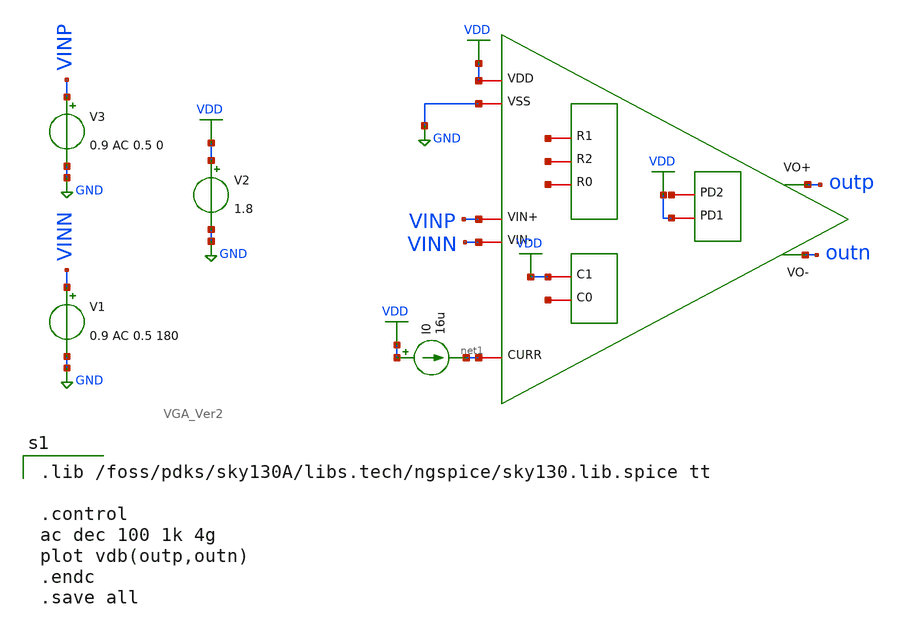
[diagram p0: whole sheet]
** sch_path: VGA/VGA_Ver2_tb.sch
**.subckt VGA_Ver2_tb
x1 outp outn net1 GND VDD VDD net2 VINN VINP net3 net4 net5 net6 VDD VGA_Ver2
V1 VINN GND 0.9 AC 0.5 180
V2 VDD GND 1.8
V3 VINP GND 0.9 AC 0.5 0
I0 VDD net1 16u
**** begin user architecture code

.lib /foss/pdks/sky130A/libs.tech/ngspice/sky130.lib.spice tt

.control
ac dec 100 1k 4g
plot vdb(outp,outn)
.endc
.save all


**** end user architecture code
**.ends

* expanding   symbol:  /foss/designs/VGA/VGA_Ver2.sym # of pins=14
** sym_path: VGA/VGA_Ver2.sym
** sch_path: VGA/VGA_Ver2.sch
.subckt VGA_Ver2 VO+ VO- CURR VSS VDD PD1 PD2 VIN- VIN+ R0 R2 R1 C0 C1
*.iopin VIN+
*.iopin VIN-
*.opin VO+
*.opin VO-
*.iopin VDD
*.iopin VSS
*.iopin PD1
*.iopin PD2
*.iopin CURR
*.iopin R0
*.iopin R1
*.iopin R2
*.iopin C1
*.iopin C0
XM10 net1 net9 VDD VDD sky130_fd_pr__pfet_01v8_lvt L=0.4 W=30 nf=1 ad='int((1 + 1)/2) * 30 / 1 * 0.29'
+ as='int((1 + 2)/2) * 30 / 1 * 0.29' pd='2*int((1 + 1)/2) * (30 / 1 + 0.29)' ps='2*int((1 + 2)/2) * (30 / 1 + 0.29)'
+ nrd='0.29 / 30 ' nrs='0.29 / 30 ' sa=0 sb=0 sd=0 mult=1 m=1
XM1 net2 net4 VDD VDD sky130_fd_pr__pfet_01v8_lvt L=0.4 W=30 nf=1 ad='int((1 + 1)/2) * 30 / 1 * 0.29'
+ as='int((1 + 2)/2) * 30 / 1 * 0.29' pd='2*int((1 + 1)/2) * (30 / 1 + 0.29)' ps='2*int((1 + 2)/2) * (30 / 1 + 0.29)'
+ nrd='0.29 / 30 ' nrs='0.29 / 30 ' sa=0 sb=0 sd=0 mult=1 m=1
RS net1 VO- 1000 m=1
RS1 net2 VO+ 1000 m=1
RS2 net9 VO- 1600 m=1
RS3 VO+ net4 1600 m=1
XM2 VO- VIN+ net10 VSS sky130_fd_pr__nfet_01v8_lvt L=0.2 W=11 nf=1 ad='int((1 + 1)/2) * 11 / 1 * 0.29'
+ as='int((1 + 2)/2) * 11 / 1 * 0.29' pd='2*int((1 + 1)/2) * (11 / 1 + 0.29)' ps='2*int((1 + 2)/2) * (11 / 1 + 0.29)'
+ nrd='0.29 / 11 ' nrs='0.29 / 11 ' sa=0 sb=0 sd=0 mult=1 m=1
XM3 VO+ VIN- net3 VSS sky130_fd_pr__nfet_01v8_lvt L=0.2 W=11 nf=1 ad='int((1 + 1)/2) * 11 / 1 * 0.29'
+ as='int((1 + 2)/2) * 11 / 1 * 0.29' pd='2*int((1 + 1)/2) * (11 / 1 + 0.29)' ps='2*int((1 + 2)/2) * (11 / 1 + 0.29)'
+ nrd='0.29 / 11 ' nrs='0.29 / 11 ' sa=0 sb=0 sd=0 mult=1 m=1
x1 C1 C0 net3 net10 Cs_Banks
XM4 net10 CURR VSS VSS sky130_fd_pr__nfet_01v8_lvt L=1 W=2 nf=1 ad='int((1 + 1)/2) * 2 / 1 * 0.29' as='int((1 + 2)/2) * 2 / 1 * 0.29'
+ pd='2*int((1 + 1)/2) * (2 / 1 + 0.29)' ps='2*int((1 + 2)/2) * (2 / 1 + 0.29)' nrd='0.29 / 2 ' nrs='0.29 / 2 '
+ sa=0 sb=0 sd=0 mult=8 m=8
XM5 net3 CURR VSS VSS sky130_fd_pr__nfet_01v8_lvt L=1 W=2 nf=1 ad='int((1 + 1)/2) * 2 / 1 * 0.29' as='int((1 + 2)/2) * 2 / 1 * 0.29'
+ pd='2*int((1 + 1)/2) * (2 / 1 + 0.29)' ps='2*int((1 + 2)/2) * (2 / 1 + 0.29)' nrd='0.29 / 2 ' nrs='0.29 / 2 '
+ sa=0 sb=0 sd=0 mult=8 m=8
XM6 net2 net1 net5 VSS sky130_fd_pr__nfet_01v8_lvt L=0.2 W=4.72 nf=1 ad='int((1 + 1)/2) * 4.72 / 1 * 0.29'
+ as='int((1 + 2)/2) * 4.72 / 1 * 0.29' pd='2*int((1 + 1)/2) * (4.72 / 1 + 0.29)' ps='2*int((1 + 2)/2) * (4.72 / 1 + 0.29)'
+ nrd='0.29 / 4.72 ' nrs='0.29 / 4.72 ' sa=0 sb=0 sd=0 mult=1 m=1
XM7 net1 net2 net6 VSS sky130_fd_pr__nfet_01v8_lvt L=0.15 W=4.72 nf=1 ad='int((1 + 1)/2) * 4.72 / 1 * 0.29'
+ as='int((1 + 2)/2) * 4.72 / 1 * 0.29' pd='2*int((1 + 1)/2) * (4.72 / 1 + 0.29)' ps='2*int((1 + 2)/2) * (4.72 / 1 + 0.29)'
+ nrd='0.29 / 4.72 ' nrs='0.29 / 4.72 ' sa=0 sb=0 sd=0 mult=1 m=1
XM8 CURR CURR VSS VSS sky130_fd_pr__nfet_01v8_lvt L=1 W=2 nf=1 ad='int((1 + 1)/2) * 2 / 1 * 0.29' as='int((1 + 2)/2) * 2 / 1 * 0.29'
+ pd='2*int((1 + 1)/2) * (2 / 1 + 0.29)' ps='2*int((1 + 2)/2) * (2 / 1 + 0.29)' nrd='0.29 / 2 ' nrs='0.29 / 2 '
+ sa=0 sb=0 sd=0 mult=1 m=1
x3 R2 R1 R0 VDD net3 net10 Rs_Banks
C2 net6 net5 43.7f m=1
C1 net11 VSS 20f m=1
C3 VO- VSS 20f m=1
XM9 net5 net7 VSS VSS sky130_fd_pr__nfet_01v8_lvt L=1 W=7 nf=1 ad='int((1 + 1)/2) * 7 / 1 * 0.29' as='int((1 + 2)/2) * 7 / 1 * 0.29'
+ pd='2*int((1 + 1)/2) * (7 / 1 + 0.29)' ps='2*int((1 + 2)/2) * (7 / 1 + 0.29)' nrd='0.29 / 7 ' nrs='0.29 / 7 '
+ sa=0 sb=0 sd=0 mult=1 m=1
XM11 CURR PD1 net7 VSS sky130_fd_pr__nfet_01v8_lvt L=0.2 W=15 nf=1 ad='int((1 + 1)/2) * 15 / 1 * 0.29'
+ as='int((1 + 2)/2) * 15 / 1 * 0.29' pd='2*int((1 + 1)/2) * (15 / 1 + 0.29)' ps='2*int((1 + 2)/2) * (15 / 1 + 0.29)'
+ nrd='0.29 / 15 ' nrs='0.29 / 15 ' sa=0 sb=0 sd=0 mult=1 m=1
XM12 net7 PD2 VSS VSS sky130_fd_pr__nfet_01v8_lvt L=0.2 W=15 nf=1 ad='int((1 + 1)/2) * 15 / 1 * 0.29'
+ as='int((1 + 2)/2) * 15 / 1 * 0.29' pd='2*int((1 + 1)/2) * (15 / 1 + 0.29)' ps='2*int((1 + 2)/2) * (15 / 1 + 0.29)'
+ nrd='0.29 / 15 ' nrs='0.29 / 15 ' sa=0 sb=0 sd=0 mult=1 m=1
XM13 net6 net8 VSS VSS sky130_fd_pr__nfet_01v8_lvt L=1 W=7 nf=1 ad='int((1 + 1)/2) * 7 / 1 * 0.29' as='int((1 + 2)/2) * 7 / 1 * 0.29'
+ pd='2*int((1 + 1)/2) * (7 / 1 + 0.29)' ps='2*int((1 + 2)/2) * (7 / 1 + 0.29)' nrd='0.29 / 7 ' nrs='0.29 / 7 '
+ sa=0 sb=0 sd=0 mult=1 m=1
XM14 CURR PD1 net8 VSS sky130_fd_pr__nfet_01v8_lvt L=0.2 W=15 nf=1 ad='int((1 + 1)/2) * 15 / 1 * 0.29'
+ as='int((1 + 2)/2) * 15 / 1 * 0.29' pd='2*int((1 + 1)/2) * (15 / 1 + 0.29)' ps='2*int((1 + 2)/2) * (15 / 1 + 0.29)'
+ nrd='0.29 / 15 ' nrs='0.29 / 15 ' sa=0 sb=0 sd=0 mult=1 m=1
XM15 net8 PD2 VSS VSS sky130_fd_pr__nfet_01v8_lvt L=0.2 W=15 nf=1 ad='int((1 + 1)/2) * 15 / 1 * 0.29'
+ as='int((1 + 2)/2) * 15 / 1 * 0.29' pd='2*int((1 + 1)/2) * (15 / 1 + 0.29)' ps='2*int((1 + 2)/2) * (15 / 1 + 0.29)'
+ nrd='0.29 / 15 ' nrs='0.29 / 15 ' sa=0 sb=0 sd=0 mult=1 m=1
XM16 CURR CURR VSS VSS sky130_fd_pr__nfet_01v8_lvt L=1 W=2 nf=1 ad='int((1 + 1)/2) * 2 / 1 * 0.29' as='int((1 + 2)/2) * 2 / 1 * 0.29'
+ pd='2*int((1 + 1)/2) * (2 / 1 + 0.29)' ps='2*int((1 + 2)/2) * (2 / 1 + 0.29)' nrd='0.29 / 2 ' nrs='0.29 / 2 '
+ sa=0 sb=0 sd=0 mult=1 m=1
C4 VDD net9 20f m=1
C5 net12 net4 20f m=1
.ends


* expanding   symbol:  /foss/designs/VGA/Cs_Banks.sym # of pins=4
** sym_path: VGA/Cs_Banks.sym
** sch_path: VGA/Cs_Banks.sch
.subckt Cs_Banks C1 C0 VS2 VS1
*.iopin VS1
*.iopin VS2
*.iopin C0
*.iopin C1
XM1 net1 C1 VS1 GND sky130_fd_pr__nfet_01v8_lvt L=0.15 W=20 nf=1 ad='int((1 + 1)/2) * 20 / 1 * 0.29'
+ as='int((1 + 2)/2) * 20 / 1 * 0.29' pd='2*int((1 + 1)/2) * (20 / 1 + 0.29)' ps='2*int((1 + 2)/2) * (20 / 1 + 0.29)'
+ nrd='0.29 / 20 ' nrs='0.29 / 20 ' sa=0 sb=0 sd=0 mult=1 m=1
XM3 net3 C0 VS1 GND sky130_fd_pr__nfet_01v8_lvt L=0.15 W=20 nf=1 ad='int((1 + 1)/2) * 20 / 1 * 0.29'
+ as='int((1 + 2)/2) * 20 / 1 * 0.29' pd='2*int((1 + 1)/2) * (20 / 1 + 0.29)' ps='2*int((1 + 2)/2) * (20 / 1 + 0.29)'
+ nrd='0.29 / 20 ' nrs='0.29 / 20 ' sa=0 sb=0 sd=0 mult=1 m=1
C2 net2 net1 408f m=1
C1 net4 net3 307f m=1
XM2 net2 C1 VS2 GND sky130_fd_pr__nfet_01v8_lvt L=0.15 W=20 nf=1 ad='int((1 + 1)/2) * 20 / 1 * 0.29'
+ as='int((1 + 2)/2) * 20 / 1 * 0.29' pd='2*int((1 + 1)/2) * (20 / 1 + 0.29)' ps='2*int((1 + 2)/2) * (20 / 1 + 0.29)'
+ nrd='0.29 / 20 ' nrs='0.29 / 20 ' sa=0 sb=0 sd=0 mult=1 m=1
XM4 net4 C0 VS2 GND sky130_fd_pr__nfet_01v8_lvt L=0.15 W=20 nf=1 ad='int((1 + 1)/2) * 20 / 1 * 0.29'
+ as='int((1 + 2)/2) * 20 / 1 * 0.29' pd='2*int((1 + 1)/2) * (20 / 1 + 0.29)' ps='2*int((1 + 2)/2) * (20 / 1 + 0.29)'
+ nrd='0.29 / 20 ' nrs='0.29 / 20 ' sa=0 sb=0 sd=0 mult=1 m=1
.ends


* expanding   symbol:  /foss/designs/VGA/Rs_Banks.sym # of pins=6
** sym_path: VGA/Rs_Banks.sym
** sch_path: VGA/Rs_Banks.sch
.subckt Rs_Banks R2 R1 R0 VDD VS2 VS1
*.iopin R2
*.iopin R1
*.iopin R0
*.iopin VDD
*.iopin VS1
*.iopin VS2
XM1 VS2 VDD VS1 GND sky130_fd_pr__nfet_01v8_lvt L=0.15 W=4 nf=1 ad='int((1 + 1)/2) * 4 / 1 * 0.29' as='int((1 + 2)/2) * 4 / 1 * 0.29'
+ pd='2*int((1 + 1)/2) * (4 / 1 + 0.29)' ps='2*int((1 + 2)/2) * (4 / 1 + 0.29)' nrd='0.29 / 4 ' nrs='0.29 / 4 '
+ sa=0 sb=0 sd=0 mult=1 m=1
XM2 VS2 R0 VS1 GND sky130_fd_pr__nfet_01v8_lvt L=0.15 W=4 nf=1 ad='int((1 + 1)/2) * 4 / 1 * 0.29' as='int((1 + 2)/2) * 4 / 1 * 0.29'
+ pd='2*int((1 + 1)/2) * (4 / 1 + 0.29)' ps='2*int((1 + 2)/2) * (4 / 1 + 0.29)' nrd='0.29 / 4 ' nrs='0.29 / 4 '
+ sa=0 sb=0 sd=0 mult=1 m=1
XM3 VS2 R1 VS1 GND sky130_fd_pr__nfet_01v8_lvt L=0.15 W=4 nf=1 ad='int((1 + 1)/2) * 4 / 1 * 0.29' as='int((1 + 2)/2) * 4 / 1 * 0.29'
+ pd='2*int((1 + 1)/2) * (4 / 1 + 0.29)' ps='2*int((1 + 2)/2) * (4 / 1 + 0.29)' nrd='0.29 / 4 ' nrs='0.29 / 4 '
+ sa=0 sb=0 sd=0 mult=1 m=1
XM4 VS2 R2 VS1 GND sky130_fd_pr__nfet_01v8_lvt L=0.15 W=4 nf=1 ad='int((1 + 1)/2) * 4 / 1 * 0.29' as='int((1 + 2)/2) * 4 / 1 * 0.29'
+ pd='2*int((1 + 1)/2) * (4 / 1 + 0.29)' ps='2*int((1 + 2)/2) * (4 / 1 + 0.29)' nrd='0.29 / 4 ' nrs='0.29 / 4 '
+ sa=0 sb=0 sd=0 mult=1 m=1
.ends

.GLOBAL GND
.GLOBAL VDD
.end
